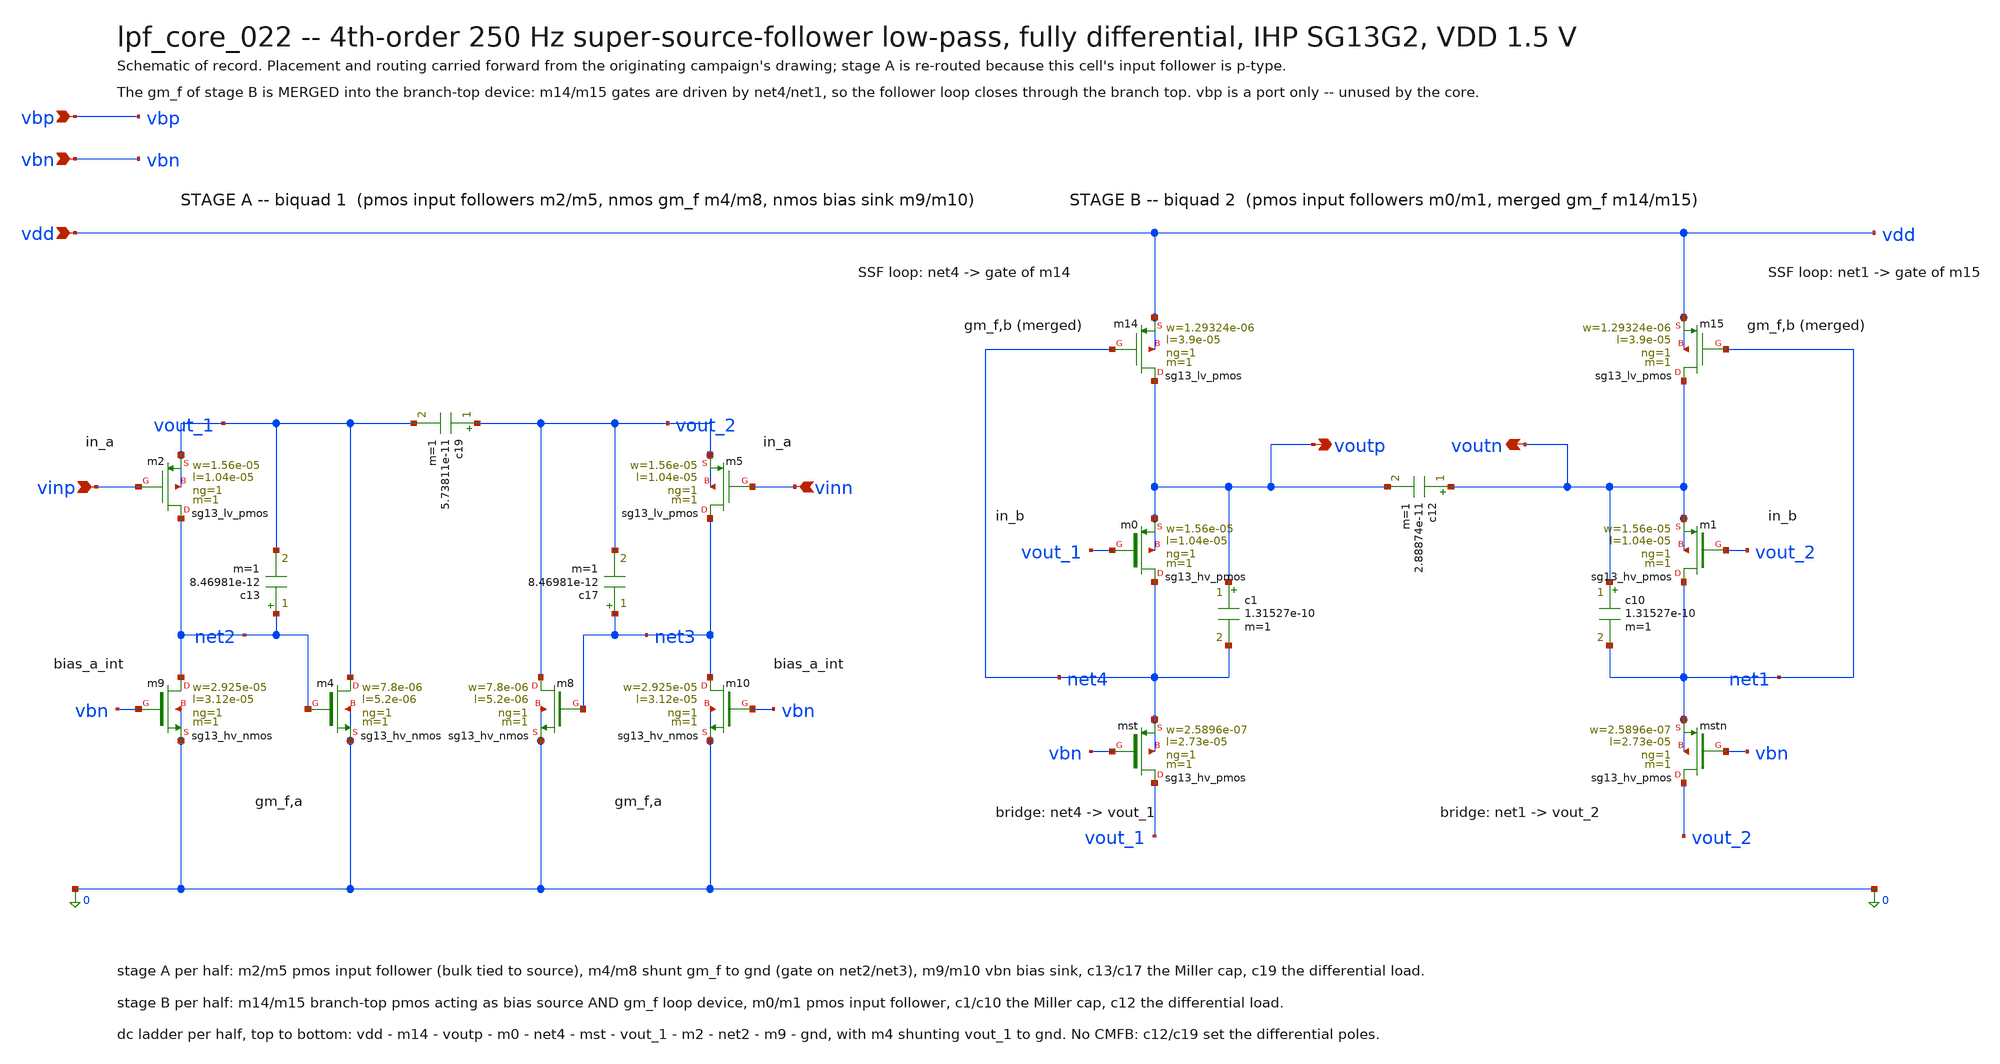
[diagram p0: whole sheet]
** sch_path: signoff/schematic/lpf_core_022.sch
**.subckt lpf_core_022 vinp vinn voutp voutn vdd vbp vbn
*.ipin vinp
*.ipin vinn
*.opin voutp
*.opin voutn
*.ipin vdd
*.ipin vbp
*.ipin vbn
Xm2 net2 vinp vout_1 vout_1 sg13_lv_pmos w=1.56e-05 l=1.04e-05 ng=1 m=1 mm_ok=1
Xm9 net2 vbn 0 0 sg13_hv_nmos w=2.925e-05 l=3.12e-05 ng=1 m=1 mm_ok=1
Xm4 vout_1 net2 0 0 sg13_hv_nmos w=7.8e-06 l=5.2e-06 ng=1 m=1 mm_ok=1
Xm5 net3 vinn vout_2 vout_2 sg13_lv_pmos w=1.56e-05 l=1.04e-05 ng=1 m=1 mm_ok=1
Xm10 net3 vbn 0 0 sg13_hv_nmos w=2.925e-05 l=3.12e-05 ng=1 m=1 mm_ok=1
Xm8 vout_2 net3 0 0 sg13_hv_nmos w=7.8e-06 l=5.2e-06 ng=1 m=1 mm_ok=1
Xm14 voutp net4 vdd vdd sg13_lv_pmos w=1.29324e-06 l=3.9e-05 ng=1 m=1 mm_ok=1
Xm0 net4 vout_1 voutp voutp sg13_hv_pmos w=1.56e-05 l=1.04e-05 ng=1 m=1 mm_ok=1
Xmst vout_1 vbn net4 net4 sg13_hv_pmos w=2.5896e-07 l=2.73e-05 ng=1 m=1 mm_ok=1
Xm15 voutn net1 vdd vdd sg13_lv_pmos w=1.29324e-06 l=3.9e-05 ng=1 m=1 mm_ok=1
Xm1 net1 vout_2 voutn voutn sg13_hv_pmos w=1.56e-05 l=1.04e-05 ng=1 m=1 mm_ok=1
Xmstn vout_2 vbn net1 net1 sg13_hv_pmos w=2.5896e-07 l=2.73e-05 ng=1 m=1 mm_ok=1
c13 net2 vout_1 8.46981e-12 m=1
c17 net3 vout_2 8.46981e-12 m=1
c19 vout_2 vout_1 5.73811e-11 m=1
c1 voutp net4 1.31527e-10 m=1
c10 voutn net1 1.31527e-10 m=1
c12 voutn voutp 2.88874e-11 m=1
**.ends
.end
